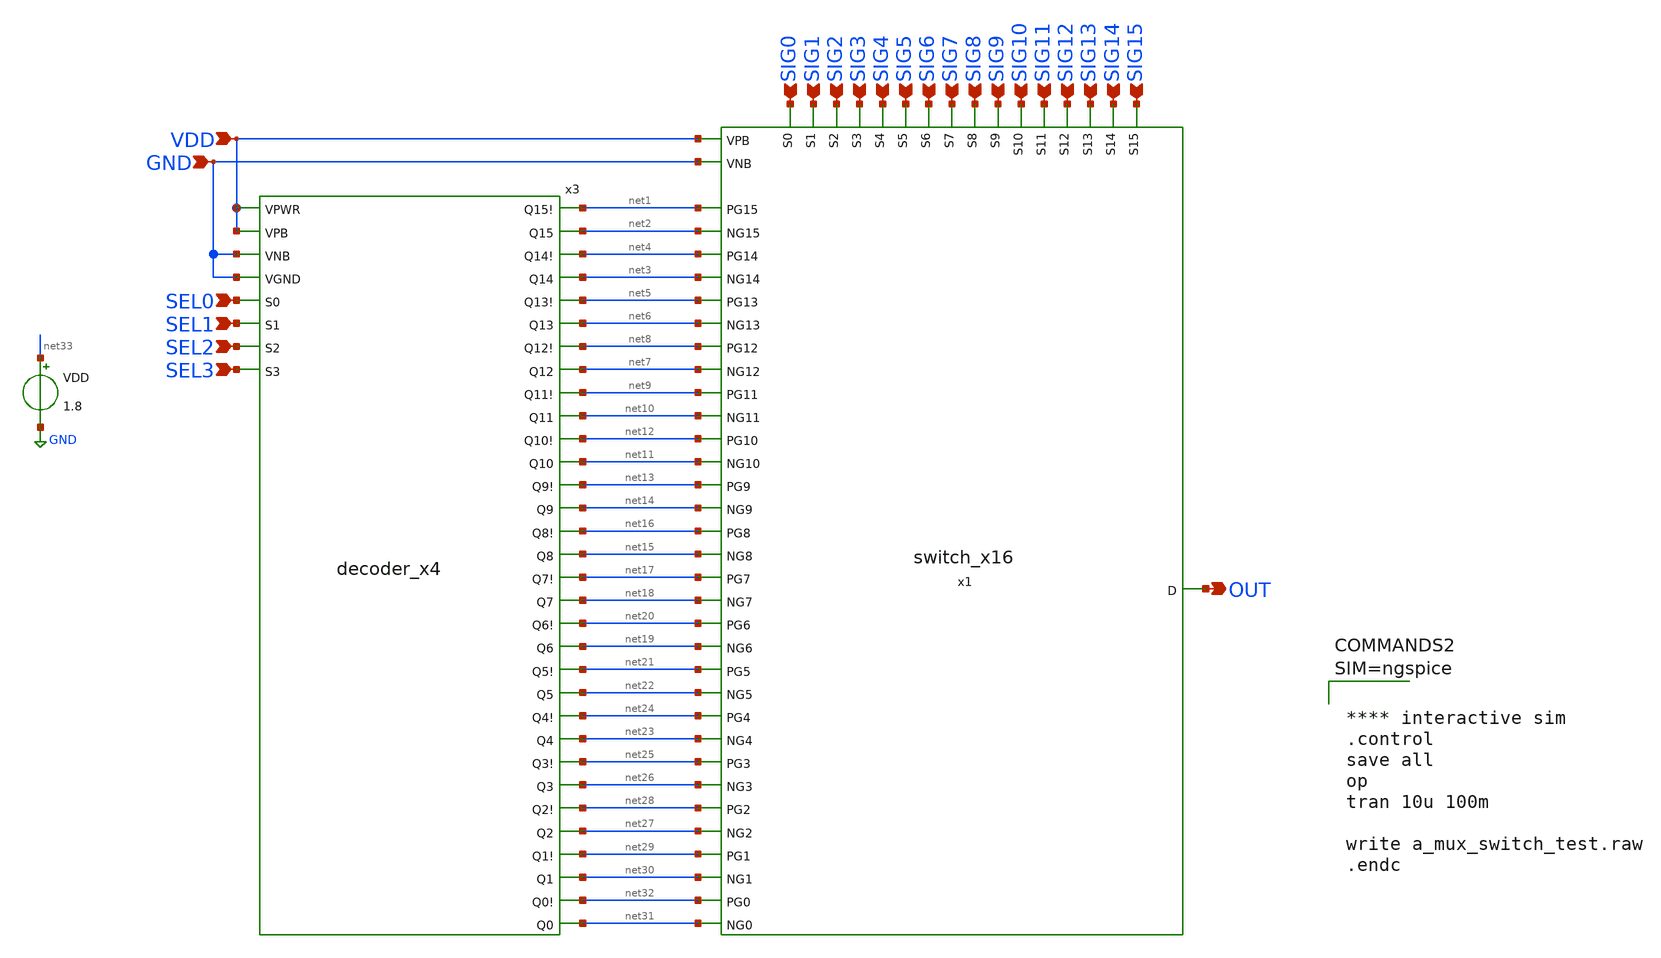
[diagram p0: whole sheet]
** sch_path: analog_mux_files 2/analog_mux.sch
**.subckt analog_mux OUT VDD GND SEL0 SEL1 SEL2 SEL3 SIG3 SIG2 SIG1 SIG0 SIG7 SIG6 SIG5 SIG4 SIG11
*+ SIG10 SIG9 SIG8 SIG15 SIG14 SIG13 SIG12
*.opin OUT
*.ipin VDD
*.ipin GND
*.ipin SEL0
*.ipin SEL1
*.ipin SEL2
*.ipin SEL3
*.ipin SIG3
*.ipin SIG2
*.ipin SIG1
*.ipin SIG0
*.ipin SIG7
*.ipin SIG6
*.ipin SIG5
*.ipin SIG4
*.ipin SIG11
*.ipin SIG10
*.ipin SIG9
*.ipin SIG8
*.ipin SIG15
*.ipin SIG14
*.ipin SIG13
*.ipin SIG12
x3 VDD VDD GND GND SEL0 SEL1 SEL2 SEL3 net1 net2 net4 net3 net5 net6 net8 net7 net9 net10 net12
+ net11 net13 net14 net16 net15 net17 net18 net20 net19 net21 net22 net24 net23 net25 net26 net28 net27
+ net29 net30 net32 net31 decoder_x4
x1 SIG15 net1 net2 SIG14 net4 net3 SIG13 net5 net6 SIG12 net8 net7 SIG11 net9 net10 SIG10 net12
+ net11 SIG9 net13 net14 SIG8 net16 net15 OUT SIG7 net17 net18 SIG6 net20 net19 SIG5 net21 net22 SIG4 net24
+ net23 SIG3 net25 net26 SIG2 net28 net27 SIG1 net29 net30 SIG0 net32 net31 VDD GND switch_x16
VDD net33 GND 1.8
**** begin user architecture code

** opencircuitdesign pdks install
.lib $::SKYWATER_MODELS/sky130.lib.spice tt
.include $::SKYWATER_STDCELLS/sky130_fd_sc_hd.spice





**** interactive sim
.control
save all
op
tran 10u 100m

write a_mux_switch_test.raw
.endc



**** end user architecture code
**.ends

* expanding   symbol:  compiled 2/decoder_x4.sym # of pins=40
** sym_path: compiled 2/decoder_x4.sym
** sch_path: compiled 2/decoder_x4.sch
.subckt decoder_x4 VPWR VPB VNB VGND S0 S1 S2 S3 Q15! Q15 Q14! Q14 Q13! Q13 Q12! Q12 Q11! Q11 Q10!
+ Q10 Q9! Q9 Q8! Q8 Q7! Q7 Q6! Q6 Q5! Q5 Q4! Q4 Q3! Q3 Q2! Q2 Q1! Q1 Q0! Q0
*.ipin S0
*.ipin S1
*.ipin S2
*.ipin S3
*.ipin VGND
*.ipin VPWR
*.ipin VNB
*.ipin VPB
*.opin Q14!
*.opin Q15!
*.opin Q13!
*.opin Q12!
*.opin Q10!
*.opin Q11!
*.opin Q9!
*.opin Q8!
*.opin Q7!
*.opin Q6!
*.opin Q4!
*.opin Q3!
*.opin Q2!
*.opin Q1!
*.opin Q0!
*.opin Q5!
*.opin Q14
*.opin Q15
*.opin Q13
*.opin Q12
*.opin Q10
*.opin Q11
*.opin Q9
*.opin Q8
*.opin Q7
*.opin Q6
*.opin Q4
*.opin Q3
*.opin Q2
*.opin Q1
*.opin Q0
*.opin Q5
x1 S0 S1 S2 S3 VGND VNB VPB VPWR Q15! sky130_fd_sc_hd__nand4_2
x2 S0 S1 S2 net1 VGND VNB VPB VPWR Q14! sky130_fd_sc_hd__nand4_2
x3 S0 S1 net2 S3 VGND VNB VPB VPWR Q13! sky130_fd_sc_hd__nand4_2
x4 S0 S1 net2 net1 VGND VNB VPB VPWR Q12! sky130_fd_sc_hd__nand4_2
x5 S0 net3 S2 S3 VGND VNB VPB VPWR Q11! sky130_fd_sc_hd__nand4_2
x6 S0 net3 S2 net1 VGND VNB VPB VPWR Q10! sky130_fd_sc_hd__nand4_2
x7 S0 net3 net2 S3 VGND VNB VPB VPWR Q9! sky130_fd_sc_hd__nand4_2
x8 S0 net3 net2 net1 VGND VNB VPB VPWR Q8! sky130_fd_sc_hd__nand4_2
x9 net4 S1 S2 S3 VGND VNB VPB VPWR Q7! sky130_fd_sc_hd__nand4_2
x10 net4 S1 S2 net1 VGND VNB VPB VPWR Q6! sky130_fd_sc_hd__nand4_2
x11 net4 S1 net2 S3 VGND VNB VPB VPWR Q5! sky130_fd_sc_hd__nand4_2
x12 net4 S1 net2 net1 VGND VNB VPB VPWR Q4! sky130_fd_sc_hd__nand4_2
x13 net4 net3 S2 S3 VGND VNB VPB VPWR Q3! sky130_fd_sc_hd__nand4_2
x14 net4 net3 S2 net1 VGND VNB VPB VPWR Q2! sky130_fd_sc_hd__nand4_2
x15 net4 net3 net2 S3 VGND VNB VPB VPWR Q1! sky130_fd_sc_hd__nand4_2
x16 net4 net3 net2 net1 VGND VNB VPB VPWR Q0! sky130_fd_sc_hd__nand4_2
x17 S0 VGND VNB VPB VPWR net4 sky130_fd_sc_hd__inv_8
x18 S1 VGND VNB VPB VPWR net3 sky130_fd_sc_hd__inv_8
x19 S2 VGND VNB VPB VPWR net2 sky130_fd_sc_hd__inv_8
x20 S3 VGND VNB VPB VPWR net1 sky130_fd_sc_hd__inv_8
x21 Q15! VGND VNB VPB VPWR Q15 sky130_fd_sc_hd__inv_1
x22 Q14! VGND VNB VPB VPWR Q14 sky130_fd_sc_hd__inv_1
x23 Q13! VGND VNB VPB VPWR Q13 sky130_fd_sc_hd__inv_1
x24 Q12! VGND VNB VPB VPWR Q12 sky130_fd_sc_hd__inv_1
x25 Q11! VGND VNB VPB VPWR Q11 sky130_fd_sc_hd__inv_1
x26 Q10! VGND VNB VPB VPWR Q10 sky130_fd_sc_hd__inv_1
x27 Q9! VGND VNB VPB VPWR Q9 sky130_fd_sc_hd__inv_1
x28 Q8! VGND VNB VPB VPWR Q8 sky130_fd_sc_hd__inv_1
x29 Q7! VGND VNB VPB VPWR Q7 sky130_fd_sc_hd__inv_1
x30 Q6! VGND VNB VPB VPWR Q6 sky130_fd_sc_hd__inv_1
x31 Q5! VGND VNB VPB VPWR Q5 sky130_fd_sc_hd__inv_1
x32 Q4! VGND VNB VPB VPWR Q4 sky130_fd_sc_hd__inv_1
x33 Q3! VGND VNB VPB VPWR Q3 sky130_fd_sc_hd__inv_1
x34 Q2! VGND VNB VPB VPWR Q2 sky130_fd_sc_hd__inv_1
x35 Q1! VGND VNB VPB VPWR Q1 sky130_fd_sc_hd__inv_1
x36 Q0! VGND VNB VPB VPWR Q0 sky130_fd_sc_hd__inv_1
.ends


* expanding   symbol:  analog_mux_files 2/switch_x16.sym # of pins=51
** sym_path: analog_mux_files 2/switch_x16.sym
** sch_path: analog_mux_files 2/switch_x16.sch
.subckt switch_x16 S15 PG15 NG15 S14 PG14 NG14 S13 PG13 NG13 S12 PG12 NG12 S11 PG11 NG11 S10 PG10
+ NG10 S9 PG9 NG9 S8 PG8 NG8 D S7 PG7 NG7 S6 PG6 NG6 S5 PG5 NG5 S4 PG4 NG4 S3 PG3 NG3 S2 PG2 NG2 S1 PG1
+ NG1 S0 PG0 NG0 VPB VNB
*.ipin PG0
*.ipin NG0
*.ipin S0
*.ipin PG1
*.ipin NG1
*.ipin S1
*.ipin PG2
*.ipin NG2
*.ipin S2
*.ipin PG3
*.ipin NG3
*.ipin S3
*.ipin PG4
*.ipin NG4
*.ipin S4
*.ipin PG5
*.ipin NG5
*.ipin S5
*.ipin PG6
*.ipin NG6
*.ipin S6
*.ipin PG7
*.ipin NG7
*.ipin S7
*.ipin PG8
*.ipin NG8
*.ipin S8
*.ipin PG9
*.ipin NG9
*.ipin S9
*.ipin PG10
*.ipin NG10
*.ipin S10
*.ipin PG11
*.ipin NG11
*.ipin S11
*.ipin PG12
*.ipin NG12
*.ipin S12
*.ipin PG13
*.ipin NG13
*.ipin S13
*.ipin PG14
*.ipin NG14
*.ipin S14
*.ipin PG15
*.ipin NG15
*.ipin S15
*.opin D
*.ipin VPB
*.ipin VNB
x1 VNB NG0 VPB PG0 S0 D a_mux_switch
x2 VNB NG1 VPB PG1 S1 D a_mux_switch
x3 VNB NG2 VPB PG2 S2 D a_mux_switch
x4 VNB NG3 VPB PG3 S3 D a_mux_switch
x5 VNB NG4 VPB PG4 S4 D a_mux_switch
x6 VNB NG5 VPB PG5 S5 D a_mux_switch
x7 VNB NG6 VPB PG6 S6 D a_mux_switch
x8 VNB NG7 VPB PG7 S7 D a_mux_switch
x9 VNB NG8 VPB PG8 S8 D a_mux_switch
x10 VNB NG9 VPB PG9 S9 D a_mux_switch
x11 VNB NG10 VPB PG10 S10 D a_mux_switch
x12 VNB NG11 VPB PG11 S11 D a_mux_switch
x13 VNB NG12 VPB PG12 S12 D a_mux_switch
x14 VNB NG13 VPB PG13 S13 D a_mux_switch
x15 VNB NG14 VPB PG14 S14 D a_mux_switch
x16 VNB NG15 VPB PG15 S15 D a_mux_switch
.ends


* expanding   symbol:  analog_mux_files/a_mux_switch.sym # of pins=6
** sym_path: analog_mux_files 2/a_mux_switch.sym
** sch_path: analog_mux_files 2/a_mux_switch.sch
.subckt a_mux_switch VNB VNG VPB VPG VS VD
*.ipin VPG
*.ipin VNG
*.ipin VS
*.opin VD
*.ipin VPB
*.ipin VNB
XM1 VD VPG VS VPB sky130_fd_pr__pfet_01v8 L=0.15 W=20 nf=1 ad='int((nf+1)/2) * W/nf * 0.29' as='int((nf+2)/2) * W/nf * 0.29'
+ pd='2*int((nf+1)/2) * (W/nf + 0.29)' ps='2*int((nf+2)/2) * (W/nf + 0.29)' nrd='0.29 / W' nrs='0.29 / W'
+ sa=0 sb=0 sd=0 mult=1 m=1
XM2 VD VNG VS VNB sky130_fd_pr__nfet_01v8 L=0.15 W=20 nf=1 ad='int((nf+1)/2) * W/nf * 0.29' as='int((nf+2)/2) * W/nf * 0.29'
+ pd='2*int((nf+1)/2) * (W/nf + 0.29)' ps='2*int((nf+2)/2) * (W/nf + 0.29)' nrd='0.29 / W' nrs='0.29 / W'
+ sa=0 sb=0 sd=0 mult=1 m=1
.ends

.GLOBAL GND
.GLOBAL VPB
.GLOBAL VNB
.end
